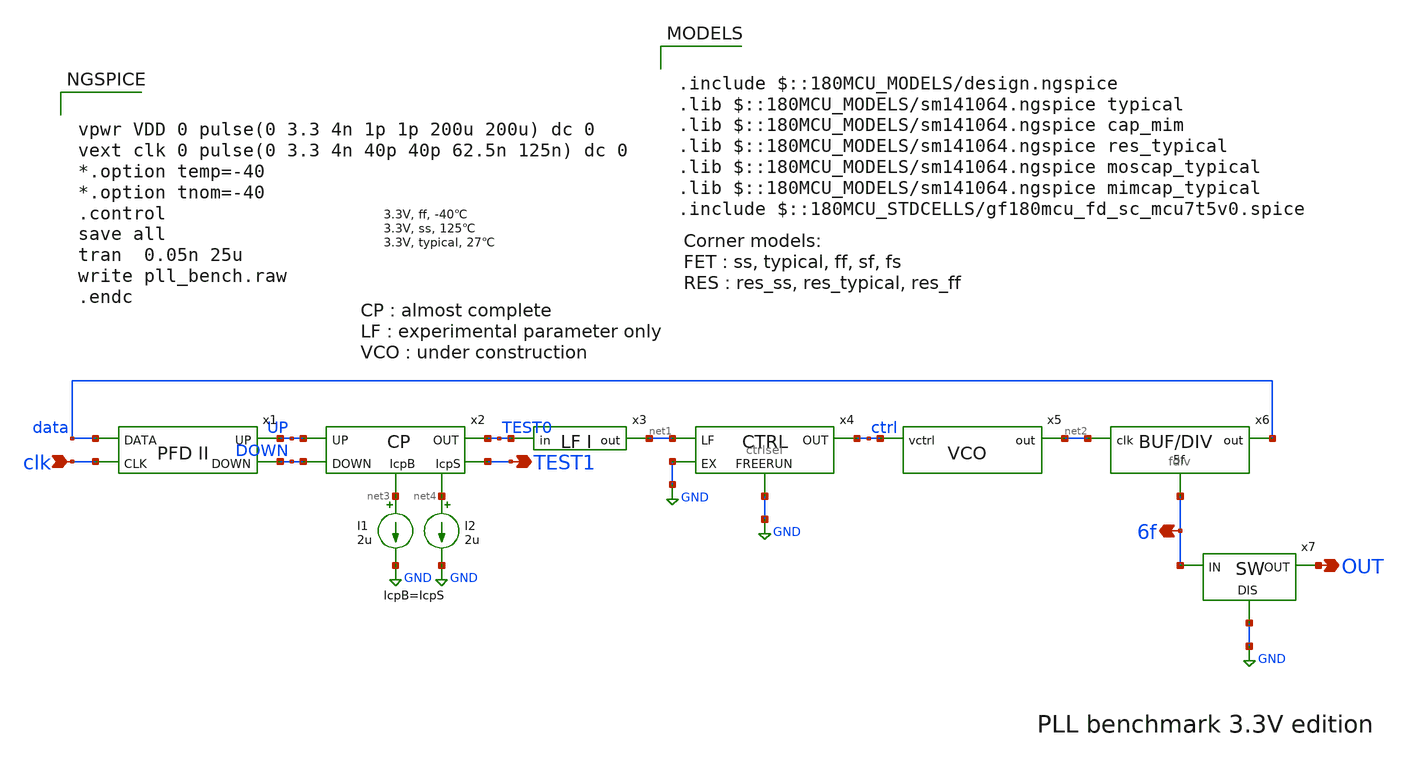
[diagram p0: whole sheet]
** sch_path: PLL/xschem/pll_bench.sch
**.subckt pll_bench clk OUT 6f TEST1
*.ipin clk
*.opin OUT
*.opin 6f
*.opin TEST1
x2 UP DOWN TEST0 net3 net4 TEST1 cp
x5 ctrl net2 vco
x3 net1 TEST0 lf
x4 GND GND ctrl net1 ctrlsel
x7 6f OUT GND sw
x1 data UP DOWN clk pfd2
I2 net4 GND 2u
I1 net3 GND 2u
x6 data net2 6f fdiv
**** begin user architecture code


vpwr VDD 0 pulse(0 3.3 4n 1p 1p 200u 200u) dc 0
vext clk 0 pulse(0 3.3 4n 40p 40p 62.5n 125n) dc 0
*.option temp=-40
*.option tnom=-40
.control
save all
tran  0.05n 25u
write pll_bench.raw
.endc



.include $::180MCU_MODELS/design.ngspice
.lib $::180MCU_MODELS/sm141064.ngspice typical
.lib $::180MCU_MODELS/sm141064.ngspice cap_mim
.lib $::180MCU_MODELS/sm141064.ngspice res_typical
.lib $::180MCU_MODELS/sm141064.ngspice moscap_typical
.lib $::180MCU_MODELS/sm141064.ngspice mimcap_typical
.include $::180MCU_STDCELLS/gf180mcu_fd_sc_mcu7t5v0.spice

**** end user architecture code
**.ends

* expanding   symbol:  cp.sym # of pins=6
** sym_path: PLL/xschem/cp.sym
** sch_path: PLL/xschem/cp.sch
.subckt cp UP DOWN OUT IcpB IcpS VF
*.iopin IcpS
*.iopin IcpB
*.ipin DOWN
*.ipin UP
*.opin OUT
*.opin VF
XM29 net17 OUT net19 VDD pfet_03v3 L=0.33u W=8u nf=1 ad='int((nf+1)/2) * W/nf * 0.18u' as='int((nf+2)/2) * W/nf * 0.18u'
+ pd='2*int((nf+1)/2) * (W/nf + 0.18u)' ps='2*int((nf+2)/2) * (W/nf + 0.18u)' nrd='0.18u / W' nrs='0.18u / W'
+ sa=0 sb=0 sd=0 m=1
XM32 net16 VF net19 VDD pfet_03v3 L=0.33u W=8u nf=1 ad='int((nf+1)/2) * W/nf * 0.18u' as='int((nf+2)/2) * W/nf * 0.18u'
+ pd='2*int((nf+1)/2) * (W/nf + 0.18u)' ps='2*int((nf+2)/2) * (W/nf + 0.18u)' nrd='0.18u / W' nrs='0.18u / W'
+ sa=0 sb=0 sd=0 m=1
XM15 VF UP net3 VDD pfet_03v3 L=0.33u W=8u nf=1 ad='int((nf+1)/2) * W/nf * 0.18u' as='int((nf+2)/2) * W/nf * 0.18u'
+ pd='2*int((nf+1)/2) * (W/nf + 0.18u)' ps='2*int((nf+2)/2) * (W/nf + 0.18u)' nrd='0.18u / W' nrs='0.18u / W'
+ sa=0 sb=0 sd=0 m=1
XM16 VF net2 net4 GND nfet_03v3 L=0.33u W=4u nf=1 ad='int((nf+1)/2) * W/nf * 0.18u' as='int((nf+2)/2) * W/nf * 0.18u'
+ pd='2*int((nf+1)/2) * (W/nf + 0.18u)' ps='2*int((nf+2)/2) * (W/nf + 0.18u)' nrd='0.18u / W' nrs='0.18u / W'
+ sa=0 sb=0 sd=0 m=1
XM11 net2 DOWN VDD VDD pfet_03v3 L=0.33u W=2u nf=1 ad='int((nf+1)/2) * W/nf * 0.18u' as='int((nf+2)/2) * W/nf * 0.18u'
+ pd='2*int((nf+1)/2) * (W/nf + 0.18u)' ps='2*int((nf+2)/2) * (W/nf + 0.18u)' nrd='0.18u / W' nrs='0.18u / W'
+ sa=0 sb=0 sd=0 m=1
XM12 net2 DOWN GND GND nfet_03v3 L=0.33u W=1u nf=1 ad='int((nf+1)/2) * W/nf * 0.18u' as='int((nf+2)/2) * W/nf * 0.18u'
+ pd='2*int((nf+1)/2) * (W/nf + 0.18u)' ps='2*int((nf+2)/2) * (W/nf + 0.18u)' nrd='0.18u / W' nrs='0.18u / W'
+ sa=0 sb=0 sd=0 m=1
XM17 net4 net11 net7 GND nfet_03v3 L=0.33u W=1u nf=1 ad='int((nf+1)/2) * W/nf * 0.18u' as='int((nf+2)/2) * W/nf * 0.18u'
+ pd='2*int((nf+1)/2) * (W/nf + 0.18u)' ps='2*int((nf+2)/2) * (W/nf + 0.18u)' nrd='0.18u / W' nrs='0.18u / W'
+ sa=0 sb=0 sd=0 m=1
XM18 net7 net12 GND GND nfet_03v3 L=0.33u W=1u nf=1 ad='int((nf+1)/2) * W/nf * 0.18u' as='int((nf+2)/2) * W/nf * 0.18u'
+ pd='2*int((nf+1)/2) * (W/nf + 0.18u)' ps='2*int((nf+2)/2) * (W/nf + 0.18u)' nrd='0.18u / W' nrs='0.18u / W'
+ sa=0 sb=0 sd=0 m=1
XM27 net14 IcpS VDD VDD pfet_03v3 L=0.33u W=4u nf=1 ad='int((nf+1)/2) * W/nf * 0.18u' as='int((nf+2)/2) * W/nf * 0.18u'
+ pd='2*int((nf+1)/2) * (W/nf + 0.18u)' ps='2*int((nf+2)/2) * (W/nf + 0.18u)' nrd='0.18u / W' nrs='0.18u / W'
+ sa=0 sb=0 sd=0 m=1
XM28 net19 IcpB net14 VDD pfet_03v3 L=0.33u W=4u nf=1 ad='int((nf+1)/2) * W/nf * 0.18u' as='int((nf+2)/2) * W/nf * 0.18u'
+ pd='2*int((nf+1)/2) * (W/nf + 0.18u)' ps='2*int((nf+2)/2) * (W/nf + 0.18u)' nrd='0.18u / W' nrs='0.18u / W'
+ sa=0 sb=0 sd=0 m=1
XM2 net6 IcpS VDD VDD pfet_03v3 L=0.33u W=4u nf=1 ad='int((nf+1)/2) * W/nf * 0.18u' as='int((nf+2)/2) * W/nf * 0.18u'
+ pd='2*int((nf+1)/2) * (W/nf + 0.18u)' ps='2*int((nf+2)/2) * (W/nf + 0.18u)' nrd='0.18u / W' nrs='0.18u / W'
+ sa=0 sb=0 sd=0 m=1
XM3 IcpS IcpB net6 VDD pfet_03v3 L=0.33u W=4u nf=1 ad='int((nf+1)/2) * W/nf * 0.18u' as='int((nf+2)/2) * W/nf * 0.18u'
+ pd='2*int((nf+1)/2) * (W/nf + 0.18u)' ps='2*int((nf+2)/2) * (W/nf + 0.18u)' nrd='0.18u / W' nrs='0.18u / W'
+ sa=0 sb=0 sd=0 m=1
XM1 IcpB IcpB VDD VDD pfet_03v3 L=0.33u W=0.8u nf=1 ad='int((nf+1)/2) * W/nf * 0.18u' as='int((nf+2)/2) * W/nf * 0.18u'
+ pd='2*int((nf+1)/2) * (W/nf + 0.18u)' ps='2*int((nf+2)/2) * (W/nf + 0.18u)' nrd='0.18u / W' nrs='0.18u / W'
+ sa=0 sb=0 sd=0 m=1
XM9 net12 net11 net8 GND nfet_03v3 L=0.33u W=2u nf=1 ad='int((nf+1)/2) * W/nf * 0.18u' as='int((nf+2)/2) * W/nf * 0.18u'
+ pd='2*int((nf+1)/2) * (W/nf + 0.18u)' ps='2*int((nf+2)/2) * (W/nf + 0.18u)' nrd='0.18u / W' nrs='0.18u / W'
+ sa=0 sb=0 sd=0 m=1
XM10 net8 net12 GND GND nfet_03v3 L=0.33u W=2u nf=1 ad='int((nf+1)/2) * W/nf * 0.18u' as='int((nf+2)/2) * W/nf * 0.18u'
+ pd='2*int((nf+1)/2) * (W/nf + 0.18u)' ps='2*int((nf+2)/2) * (W/nf + 0.18u)' nrd='0.18u / W' nrs='0.18u / W'
+ sa=0 sb=0 sd=0 m=1
XM7 net9 IcpS VDD VDD pfet_03v3 L=0.33u W=4u nf=1 ad='int((nf+1)/2) * W/nf * 0.18u' as='int((nf+2)/2) * W/nf * 0.18u'
+ pd='2*int((nf+1)/2) * (W/nf + 0.18u)' ps='2*int((nf+2)/2) * (W/nf + 0.18u)' nrd='0.18u / W' nrs='0.18u / W'
+ sa=0 sb=0 sd=0 m=1
XM8 net12 IcpB net9 VDD pfet_03v3 L=0.33u W=4u nf=1 ad='int((nf+1)/2) * W/nf * 0.18u' as='int((nf+2)/2) * W/nf * 0.18u'
+ pd='2*int((nf+1)/2) * (W/nf + 0.18u)' ps='2*int((nf+2)/2) * (W/nf + 0.18u)' nrd='0.18u / W' nrs='0.18u / W'
+ sa=0 sb=0 sd=0 m=1
XM4 net10 IcpS VDD VDD pfet_03v3 L=0.33u W=4u nf=1 ad='int((nf+1)/2) * W/nf * 0.18u' as='int((nf+2)/2) * W/nf * 0.18u'
+ pd='2*int((nf+1)/2) * (W/nf + 0.18u)' ps='2*int((nf+2)/2) * (W/nf + 0.18u)' nrd='0.18u / W' nrs='0.18u / W'
+ sa=0 sb=0 sd=0 m=1
XM5 net11 IcpB net10 VDD pfet_03v3 L=0.33u W=4u nf=1 ad='int((nf+1)/2) * W/nf * 0.18u' as='int((nf+2)/2) * W/nf * 0.18u'
+ pd='2*int((nf+1)/2) * (W/nf + 0.18u)' ps='2*int((nf+2)/2) * (W/nf + 0.18u)' nrd='0.18u / W' nrs='0.18u / W'
+ sa=0 sb=0 sd=0 m=1
XM6 net11 net11 GND GND nfet_03v3 L=0.33u W=0.4u nf=1 ad='int((nf+1)/2) * W/nf * 0.18u' as='int((nf+2)/2) * W/nf * 0.18u'
+ pd='2*int((nf+1)/2) * (W/nf + 0.18u)' ps='2*int((nf+2)/2) * (W/nf + 0.18u)' nrd='0.18u / W' nrs='0.18u / W'
+ sa=0 sb=0 sd=0 m=1
XM43 net22 net11 net16 GND nfet_03v3 L=0.33u W=2u nf=1 ad='int((nf+1)/2) * W/nf * 0.18u' as='int((nf+2)/2) * W/nf * 0.18u'
+ pd='2*int((nf+1)/2) * (W/nf + 0.18u)' ps='2*int((nf+2)/2) * (W/nf + 0.18u)' nrd='0.18u / W' nrs='0.18u / W'
+ sa=0 sb=0 sd=0 m=1
XM39 net15 net21 VDD VDD pfet_03v3 L=0.33u W=8u nf=1 ad='int((nf+1)/2) * W/nf * 0.18u' as='int((nf+2)/2) * W/nf * 0.18u'
+ pd='2*int((nf+1)/2) * (W/nf + 0.18u)' ps='2*int((nf+2)/2) * (W/nf + 0.18u)' nrd='0.18u / W' nrs='0.18u / W'
+ sa=0 sb=0 sd=0 m=1
XM44 net16 net22 GND GND nfet_03v3 L=0.33u W=4u nf=1 ad='int((nf+1)/2) * W/nf * 0.18u' as='int((nf+2)/2) * W/nf * 0.18u'
+ pd='2*int((nf+1)/2) * (W/nf + 0.18u)' ps='2*int((nf+2)/2) * (W/nf + 0.18u)' nrd='0.18u / W' nrs='0.18u / W'
+ sa=0 sb=0 sd=0 m=1
XM45 net18 net21 VDD VDD pfet_03v3 L=0.33u W=8u nf=1 ad='int((nf+1)/2) * W/nf * 0.18u' as='int((nf+2)/2) * W/nf * 0.18u'
+ pd='2*int((nf+1)/2) * (W/nf + 0.18u)' ps='2*int((nf+2)/2) * (W/nf + 0.18u)' nrd='0.18u / W' nrs='0.18u / W'
+ sa=0 sb=0 sd=0 m=1
XM46 net24 IcpB net18 VDD pfet_03v3 L=0.33u W=4u nf=1 ad='int((nf+1)/2) * W/nf * 0.18u' as='int((nf+2)/2) * W/nf * 0.18u'
+ pd='2*int((nf+1)/2) * (W/nf + 0.18u)' ps='2*int((nf+2)/2) * (W/nf + 0.18u)' nrd='0.18u / W' nrs='0.18u / W'
+ sa=0 sb=0 sd=0 m=1
XM49 net34 net11 net17 GND nfet_03v3 L=0.33u W=2u nf=1 ad='int((nf+1)/2) * W/nf * 0.18u' as='int((nf+2)/2) * W/nf * 0.18u'
+ pd='2*int((nf+1)/2) * (W/nf + 0.18u)' ps='2*int((nf+2)/2) * (W/nf + 0.18u)' nrd='0.18u / W' nrs='0.18u / W'
+ sa=0 sb=0 sd=0 m=1
XM50 net17 net22 GND GND nfet_03v3 L=0.33u W=4u nf=1 ad='int((nf+1)/2) * W/nf * 0.18u' as='int((nf+2)/2) * W/nf * 0.18u'
+ pd='2*int((nf+1)/2) * (W/nf + 0.18u)' ps='2*int((nf+2)/2) * (W/nf + 0.18u)' nrd='0.18u / W' nrs='0.18u / W'
+ sa=0 sb=0 sd=0 m=1
XM34 net20 net11 net13 GND nfet_03v3 L=0.33u W=2u nf=1 ad='int((nf+1)/2) * W/nf * 0.18u' as='int((nf+2)/2) * W/nf * 0.18u'
+ pd='2*int((nf+1)/2) * (W/nf + 0.18u)' ps='2*int((nf+2)/2) * (W/nf + 0.18u)' nrd='0.18u / W' nrs='0.18u / W'
+ sa=0 sb=0 sd=0 m=1
XM35 net13 net12 GND GND nfet_03v3 L=0.33u W=2u nf=1 ad='int((nf+1)/2) * W/nf * 0.18u' as='int((nf+2)/2) * W/nf * 0.18u'
+ pd='2*int((nf+1)/2) * (W/nf + 0.18u)' ps='2*int((nf+2)/2) * (W/nf + 0.18u)' nrd='0.18u / W' nrs='0.18u / W'
+ sa=0 sb=0 sd=0 m=1
XM33 net18 OUT net20 GND nfet_03v3 L=0.33u W=4u nf=1 ad='int((nf+1)/2) * W/nf * 0.18u' as='int((nf+2)/2) * W/nf * 0.18u'
+ pd='2*int((nf+1)/2) * (W/nf + 0.18u)' ps='2*int((nf+2)/2) * (W/nf + 0.18u)' nrd='0.18u / W' nrs='0.18u / W'
+ sa=0 sb=0 sd=0 m=1
XM36 net15 VF net20 GND nfet_03v3 L=0.33u W=4u nf=1 ad='int((nf+1)/2) * W/nf * 0.18u' as='int((nf+2)/2) * W/nf * 0.18u'
+ pd='2*int((nf+1)/2) * (W/nf + 0.18u)' ps='2*int((nf+2)/2) * (W/nf + 0.18u)' nrd='0.18u / W' nrs='0.18u / W'
+ sa=0 sb=0 sd=0 m=1
XM41 net22 net33 net21 VDD pfet_03v3 L=0.33u W=2u nf=1 ad='int((nf+1)/2) * W/nf * 0.18u' as='int((nf+2)/2) * W/nf * 0.18u'
+ pd='2*int((nf+1)/2) * (W/nf + 0.18u)' ps='2*int((nf+2)/2) * (W/nf + 0.18u)' nrd='0.18u / W' nrs='0.18u / W'
+ sa=0 sb=0 sd=0 m=1
XM42 net21 net23 net22 GND nfet_03v3 L=0.33u W=1u nf=1 ad='int((nf+1)/2) * W/nf * 0.18u' as='int((nf+2)/2) * W/nf * 0.18u'
+ pd='2*int((nf+1)/2) * (W/nf + 0.18u)' ps='2*int((nf+2)/2) * (W/nf + 0.18u)' nrd='0.18u / W' nrs='0.18u / W'
+ sa=0 sb=0 sd=0 m=1
XM47 net34 net33 net24 VDD pfet_03v3 L=0.33u W=2u nf=1 ad='int((nf+1)/2) * W/nf * 0.18u' as='int((nf+2)/2) * W/nf * 0.18u'
+ pd='2*int((nf+1)/2) * (W/nf + 0.18u)' ps='2*int((nf+2)/2) * (W/nf + 0.18u)' nrd='0.18u / W' nrs='0.18u / W'
+ sa=0 sb=0 sd=0 m=1
XM48 net24 net23 net34 GND nfet_03v3 L=0.33u W=1u nf=1 ad='int((nf+1)/2) * W/nf * 0.18u' as='int((nf+2)/2) * W/nf * 0.18u'
+ pd='2*int((nf+1)/2) * (W/nf + 0.18u)' ps='2*int((nf+2)/2) * (W/nf + 0.18u)' nrd='0.18u / W' nrs='0.18u / W'
+ sa=0 sb=0 sd=0 m=1
XM61 VF net24 VDD VDD pfet_03v3 L=0.33u W=8u nf=1 ad='int((nf+1)/2) * W/nf * 0.18u' as='int((nf+2)/2) * W/nf * 0.18u'
+ pd='2*int((nf+1)/2) * (W/nf + 0.18u)' ps='2*int((nf+2)/2) * (W/nf + 0.18u)' nrd='0.18u / W' nrs='0.18u / W'
+ sa=0 sb=0 sd=0 m=1
XM51 net25 net26 VDD VDD pfet_03v3 L=0.33u W=4u nf=1 ad='int((nf+1)/2) * W/nf * 0.18u' as='int((nf+2)/2) * W/nf * 0.18u'
+ pd='2*int((nf+1)/2) * (W/nf + 0.18u)' ps='2*int((nf+2)/2) * (W/nf + 0.18u)' nrd='0.18u / W' nrs='0.18u / W'
+ sa=0 sb=0 sd=0 m=1
XM52 net26 IcpB net25 VDD pfet_03v3 L=0.33u W=4u nf=1 ad='int((nf+1)/2) * W/nf * 0.18u' as='int((nf+2)/2) * W/nf * 0.18u'
+ pd='2*int((nf+1)/2) * (W/nf + 0.18u)' ps='2*int((nf+2)/2) * (W/nf + 0.18u)' nrd='0.18u / W' nrs='0.18u / W'
+ sa=0 sb=0 sd=0 m=1
XM53 net33 net33 net26 VDD pfet_03v3 L=0.33u W=4u nf=1 ad='int((nf+1)/2) * W/nf * 0.18u' as='int((nf+2)/2) * W/nf * 0.18u'
+ pd='2*int((nf+1)/2) * (W/nf + 0.18u)' ps='2*int((nf+2)/2) * (W/nf + 0.18u)' nrd='0.18u / W' nrs='0.18u / W'
+ sa=0 sb=0 sd=0 m=1
XM54 net33 net11 net27 GND nfet_03v3 L=0.33u W=2u nf=1 ad='int((nf+1)/2) * W/nf * 0.18u' as='int((nf+2)/2) * W/nf * 0.18u'
+ pd='2*int((nf+1)/2) * (W/nf + 0.18u)' ps='2*int((nf+2)/2) * (W/nf + 0.18u)' nrd='0.18u / W' nrs='0.18u / W'
+ sa=0 sb=0 sd=0 m=1
XM55 net27 net12 GND GND nfet_03v3 L=0.33u W=2u nf=1 ad='int((nf+1)/2) * W/nf * 0.18u' as='int((nf+2)/2) * W/nf * 0.18u'
+ pd='2*int((nf+1)/2) * (W/nf + 0.18u)' ps='2*int((nf+2)/2) * (W/nf + 0.18u)' nrd='0.18u / W' nrs='0.18u / W'
+ sa=0 sb=0 sd=0 m=1
XM56 net28 IcpS VDD VDD pfet_03v3 L=0.33u W=4u nf=1 ad='int((nf+1)/2) * W/nf * 0.18u' as='int((nf+2)/2) * W/nf * 0.18u'
+ pd='2*int((nf+1)/2) * (W/nf + 0.18u)' ps='2*int((nf+2)/2) * (W/nf + 0.18u)' nrd='0.18u / W' nrs='0.18u / W'
+ sa=0 sb=0 sd=0 m=1
XM57 net23 IcpB net28 VDD pfet_03v3 L=0.33u W=4u nf=1 ad='int((nf+1)/2) * W/nf * 0.18u' as='int((nf+2)/2) * W/nf * 0.18u'
+ pd='2*int((nf+1)/2) * (W/nf + 0.18u)' ps='2*int((nf+2)/2) * (W/nf + 0.18u)' nrd='0.18u / W' nrs='0.18u / W'
+ sa=0 sb=0 sd=0 m=1
XM59 net30 net11 net29 GND nfet_03v3 L=0.33u W=2u nf=1 ad='int((nf+1)/2) * W/nf * 0.18u' as='int((nf+2)/2) * W/nf * 0.18u'
+ pd='2*int((nf+1)/2) * (W/nf + 0.18u)' ps='2*int((nf+2)/2) * (W/nf + 0.18u)' nrd='0.18u / W' nrs='0.18u / W'
+ sa=0 sb=0 sd=0 m=1
XM60 net29 net30 GND GND nfet_03v3 L=0.33u W=2u nf=1 ad='int((nf+1)/2) * W/nf * 0.18u' as='int((nf+2)/2) * W/nf * 0.18u'
+ pd='2*int((nf+1)/2) * (W/nf + 0.18u)' ps='2*int((nf+2)/2) * (W/nf + 0.18u)' nrd='0.18u / W' nrs='0.18u / W'
+ sa=0 sb=0 sd=0 m=1
XM58 net23 net23 net30 GND nfet_03v3 L=0.33u W=2u nf=1 ad='int((nf+1)/2) * W/nf * 0.18u' as='int((nf+2)/2) * W/nf * 0.18u'
+ pd='2*int((nf+1)/2) * (W/nf + 0.18u)' ps='2*int((nf+2)/2) * (W/nf + 0.18u)' nrd='0.18u / W' nrs='0.18u / W'
+ sa=0 sb=0 sd=0 m=1
XM62 VF net34 GND GND nfet_03v3 L=0.33u W=4u nf=1 ad='int((nf+1)/2) * W/nf * 0.18u' as='int((nf+2)/2) * W/nf * 0.18u'
+ pd='2*int((nf+1)/2) * (W/nf + 0.18u)' ps='2*int((nf+2)/2) * (W/nf + 0.18u)' nrd='0.18u / W' nrs='0.18u / W'
+ sa=0 sb=0 sd=0 m=1
XM30 net31 IcpS VDD VDD pfet_03v3 L=0.33u W=4u nf=1 ad='int((nf+1)/2) * W/nf * 0.18u' as='int((nf+2)/2) * W/nf * 0.18u'
+ pd='2*int((nf+1)/2) * (W/nf + 0.18u)' ps='2*int((nf+2)/2) * (W/nf + 0.18u)' nrd='0.18u / W' nrs='0.18u / W'
+ sa=0 sb=0 sd=0 m=1
XM31 net19 IcpB net31 VDD pfet_03v3 L=0.33u W=4u nf=1 ad='int((nf+1)/2) * W/nf * 0.18u' as='int((nf+2)/2) * W/nf * 0.18u'
+ pd='2*int((nf+1)/2) * (W/nf + 0.18u)' ps='2*int((nf+2)/2) * (W/nf + 0.18u)' nrd='0.18u / W' nrs='0.18u / W'
+ sa=0 sb=0 sd=0 m=1
XM37 net20 net11 net32 GND nfet_03v3 L=0.33u W=2u nf=1 ad='int((nf+1)/2) * W/nf * 0.18u' as='int((nf+2)/2) * W/nf * 0.18u'
+ pd='2*int((nf+1)/2) * (W/nf + 0.18u)' ps='2*int((nf+2)/2) * (W/nf + 0.18u)' nrd='0.18u / W' nrs='0.18u / W'
+ sa=0 sb=0 sd=0 m=1
XM38 net32 net12 GND GND nfet_03v3 L=0.33u W=2u nf=1 ad='int((nf+1)/2) * W/nf * 0.18u' as='int((nf+2)/2) * W/nf * 0.18u'
+ pd='2*int((nf+1)/2) * (W/nf + 0.18u)' ps='2*int((nf+2)/2) * (W/nf + 0.18u)' nrd='0.18u / W' nrs='0.18u / W'
+ sa=0 sb=0 sd=0 m=1
C1 net18 VF 280f m=1
C2 VF net17 280f m=1
XM13 net35 IcpS VDD VDD pfet_03v3 L=0.33u W=2u nf=1 ad='int((nf+1)/2) * W/nf * 0.18u' as='int((nf+2)/2) * W/nf * 0.18u'
+ pd='2*int((nf+1)/2) * (W/nf + 0.18u)' ps='2*int((nf+2)/2) * (W/nf + 0.18u)' nrd='0.18u / W' nrs='0.18u / W'
+ sa=0 sb=0 sd=0 m=1
XM14 net3 IcpB net35 VDD pfet_03v3 L=0.33u W=2u nf=1 ad='int((nf+1)/2) * W/nf * 0.18u' as='int((nf+2)/2) * W/nf * 0.18u'
+ pd='2*int((nf+1)/2) * (W/nf + 0.18u)' ps='2*int((nf+2)/2) * (W/nf + 0.18u)' nrd='0.18u / W' nrs='0.18u / W'
+ sa=0 sb=0 sd=0 m=1
XM19 net5 IcpS VDD VDD pfet_03v3 L=0.33u W=2u nf=1 ad='int((nf+1)/2) * W/nf * 0.18u' as='int((nf+2)/2) * W/nf * 0.18u'
+ pd='2*int((nf+1)/2) * (W/nf + 0.18u)' ps='2*int((nf+2)/2) * (W/nf + 0.18u)' nrd='0.18u / W' nrs='0.18u / W'
+ sa=0 sb=0 sd=0 m=1
XM20 net3 IcpB net5 VDD pfet_03v3 L=0.33u W=2u nf=1 ad='int((nf+1)/2) * W/nf * 0.18u' as='int((nf+2)/2) * W/nf * 0.18u'
+ pd='2*int((nf+1)/2) * (W/nf + 0.18u)' ps='2*int((nf+2)/2) * (W/nf + 0.18u)' nrd='0.18u / W' nrs='0.18u / W'
+ sa=0 sb=0 sd=0 m=1
XM21 OUT net1 net3 VDD pfet_03v3 L=0.33u W=8u nf=1 ad='int((nf+1)/2) * W/nf * 0.18u' as='int((nf+2)/2) * W/nf * 0.18u'
+ pd='2*int((nf+1)/2) * (W/nf + 0.18u)' ps='2*int((nf+2)/2) * (W/nf + 0.18u)' nrd='0.18u / W' nrs='0.18u / W'
+ sa=0 sb=0 sd=0 m=1
XM22 OUT DOWN net4 GND nfet_03v3 L=0.33u W=4u nf=1 ad='int((nf+1)/2) * W/nf * 0.18u' as='int((nf+2)/2) * W/nf * 0.18u'
+ pd='2*int((nf+1)/2) * (W/nf + 0.18u)' ps='2*int((nf+2)/2) * (W/nf + 0.18u)' nrd='0.18u / W' nrs='0.18u / W'
+ sa=0 sb=0 sd=0 m=1
XM23 net4 net11 net36 GND nfet_03v3 L=0.33u W=1u nf=1 ad='int((nf+1)/2) * W/nf * 0.18u' as='int((nf+2)/2) * W/nf * 0.18u'
+ pd='2*int((nf+1)/2) * (W/nf + 0.18u)' ps='2*int((nf+2)/2) * (W/nf + 0.18u)' nrd='0.18u / W' nrs='0.18u / W'
+ sa=0 sb=0 sd=0 m=1
XM24 net36 net12 GND GND nfet_03v3 L=0.33u W=1u nf=1 ad='int((nf+1)/2) * W/nf * 0.18u' as='int((nf+2)/2) * W/nf * 0.18u'
+ pd='2*int((nf+1)/2) * (W/nf + 0.18u)' ps='2*int((nf+2)/2) * (W/nf + 0.18u)' nrd='0.18u / W' nrs='0.18u / W'
+ sa=0 sb=0 sd=0 m=1
XM25 net1 UP VDD VDD pfet_03v3 L=0.33u W=2u nf=1 ad='int((nf+1)/2) * W/nf * 0.18u' as='int((nf+2)/2) * W/nf * 0.18u'
+ pd='2*int((nf+1)/2) * (W/nf + 0.18u)' ps='2*int((nf+2)/2) * (W/nf + 0.18u)' nrd='0.18u / W' nrs='0.18u / W'
+ sa=0 sb=0 sd=0 m=1
XM26 net1 UP GND GND nfet_03v3 L=0.33u W=1u nf=1 ad='int((nf+1)/2) * W/nf * 0.18u' as='int((nf+2)/2) * W/nf * 0.18u'
+ pd='2*int((nf+1)/2) * (W/nf + 0.18u)' ps='2*int((nf+2)/2) * (W/nf + 0.18u)' nrd='0.18u / W' nrs='0.18u / W'
+ sa=0 sb=0 sd=0 m=1
XM40 net21 IcpB net15 VDD pfet_03v3 L=0.33u W=4u nf=1 ad='int((nf+1)/2) * W/nf * 0.18u' as='int((nf+2)/2) * W/nf * 0.18u'
+ pd='2*int((nf+1)/2) * (W/nf + 0.18u)' ps='2*int((nf+2)/2) * (W/nf + 0.18u)' nrd='0.18u / W' nrs='0.18u / W'
+ sa=0 sb=0 sd=0 m=1
.ends


* expanding   symbol:  vco.sym # of pins=2
** sym_path: PLL/xschem/vco.sym
** sch_path: PLL/xschem/vco.sch
.subckt vco vctrl out
*.ipin vctrl
*.opin out
XM2 net1 net1 VDD VDD pfet_03v3 L=0.33u W=2u nf=1 ad='int((nf+1)/2) * W/nf * 0.18u' as='int((nf+2)/2) * W/nf * 0.18u'
+ pd='2*int((nf+1)/2) * (W/nf + 0.18u)' ps='2*int((nf+2)/2) * (W/nf + 0.18u)' nrd='0.18u / W' nrs='0.18u / W'
+ sa=0 sb=0 sd=0 m=1
XM4 net2 net1 VDD VDD pfet_03v3 L=0.33u W=2u nf=1 ad='int((nf+1)/2) * W/nf * 0.18u' as='int((nf+2)/2) * W/nf * 0.18u'
+ pd='2*int((nf+1)/2) * (W/nf + 0.18u)' ps='2*int((nf+2)/2) * (W/nf + 0.18u)' nrd='0.18u / W' nrs='0.18u / W'
+ sa=0 sb=0 sd=0 m=1
XM1 net2 net2 GND GND nfet_03v3 L=0.33u W=0.8u nf=1 ad='int((nf+1)/2) * W/nf * 0.18u' as='int((nf+2)/2) * W/nf * 0.18u'
+ pd='2*int((nf+1)/2) * (W/nf + 0.18u)' ps='2*int((nf+2)/2) * (W/nf + 0.18u)' nrd='0.18u / W' nrs='0.18u / W'
+ sa=0 sb=0 sd=0 m=1
XM5 net6 net1 VDD VDD pfet_03v3 L=0.33u W=2u nf=1 ad='int((nf+1)/2) * W/nf * 0.18u' as='int((nf+2)/2) * W/nf * 0.18u'
+ pd='2*int((nf+1)/2) * (W/nf + 0.18u)' ps='2*int((nf+2)/2) * (W/nf + 0.18u)' nrd='0.18u / W' nrs='0.18u / W'
+ sa=0 sb=0 sd=0 m=1
XM6 net5 net2 GND GND nfet_03v3 L=0.33u W=0.8u nf=1 ad='int((nf+1)/2) * W/nf * 0.18u' as='int((nf+2)/2) * W/nf * 0.18u'
+ pd='2*int((nf+1)/2) * (W/nf + 0.18u)' ps='2*int((nf+2)/2) * (W/nf + 0.18u)' nrd='0.18u / W' nrs='0.18u / W'
+ sa=0 sb=0 sd=0 m=1
I1 VDD net3 2u
XM8 net3 net3 GND GND nfet_03v3 L=0.33u W=0.8u nf=1 ad='int((nf+1)/2) * W/nf * 0.18u' as='int((nf+2)/2) * W/nf * 0.18u'
+ pd='2*int((nf+1)/2) * (W/nf + 0.18u)' ps='2*int((nf+2)/2) * (W/nf + 0.18u)' nrd='0.18u / W' nrs='0.18u / W'
+ sa=0 sb=0 sd=0 m=1
R1 net21 GND 240k m=1
XM3 net1 vctrl net21 GND nfet_03v3 L=0.28u W=0.8u nf=1 ad='int((nf+1)/2) * W/nf * 0.18u' as='int((nf+2)/2) * W/nf * 0.18u'
+ pd='2*int((nf+1)/2) * (W/nf + 0.18u)' ps='2*int((nf+2)/2) * (W/nf + 0.18u)' nrd='0.18u / W' nrs='0.18u / W'
+ sa=0 sb=0 sd=0 m=1
XM7 net1 net3 GND GND nfet_03v3 L=0.33u W=2.4u nf=1 ad='int((nf+1)/2) * W/nf * 0.18u' as='int((nf+2)/2) * W/nf * 0.18u'
+ pd='2*int((nf+1)/2) * (W/nf + 0.18u)' ps='2*int((nf+2)/2) * (W/nf + 0.18u)' nrd='0.18u / W' nrs='0.18u / W'
+ sa=0 sb=0 sd=0 m=1
XM9 net4 out net6 VDD pfet_03v3 L=0.33u W=4u nf=1 ad='int((nf+1)/2) * W/nf * 0.18u' as='int((nf+2)/2) * W/nf * 0.18u'
+ pd='2*int((nf+1)/2) * (W/nf + 0.18u)' ps='2*int((nf+2)/2) * (W/nf + 0.18u)' nrd='0.18u / W' nrs='0.18u / W'
+ sa=0 sb=0 sd=0 m=1
XM10 net4 out net5 GND nfet_03v3 L=0.33u W=1.6u nf=1 ad='int((nf+1)/2) * W/nf * 0.18u' as='int((nf+2)/2) * W/nf * 0.18u'
+ pd='2*int((nf+1)/2) * (W/nf + 0.18u)' ps='2*int((nf+2)/2) * (W/nf + 0.18u)' nrd='0.18u / W' nrs='0.18u / W'
+ sa=0 sb=0 sd=0 m=1
XM11 net9 net1 VDD VDD pfet_03v3 L=0.33u W=2u nf=1 ad='int((nf+1)/2) * W/nf * 0.18u' as='int((nf+2)/2) * W/nf * 0.18u'
+ pd='2*int((nf+1)/2) * (W/nf + 0.18u)' ps='2*int((nf+2)/2) * (W/nf + 0.18u)' nrd='0.18u / W' nrs='0.18u / W'
+ sa=0 sb=0 sd=0 m=1
XM12 net8 net2 GND GND nfet_03v3 L=0.33u W=0.8u nf=1 ad='int((nf+1)/2) * W/nf * 0.18u' as='int((nf+2)/2) * W/nf * 0.18u'
+ pd='2*int((nf+1)/2) * (W/nf + 0.18u)' ps='2*int((nf+2)/2) * (W/nf + 0.18u)' nrd='0.18u / W' nrs='0.18u / W'
+ sa=0 sb=0 sd=0 m=1
XM13 net7 net4 net9 VDD pfet_03v3 L=0.33u W=4u nf=1 ad='int((nf+1)/2) * W/nf * 0.18u' as='int((nf+2)/2) * W/nf * 0.18u'
+ pd='2*int((nf+1)/2) * (W/nf + 0.18u)' ps='2*int((nf+2)/2) * (W/nf + 0.18u)' nrd='0.18u / W' nrs='0.18u / W'
+ sa=0 sb=0 sd=0 m=1
XM14 net7 net4 net8 GND nfet_03v3 L=0.33u W=1.6u nf=1 ad='int((nf+1)/2) * W/nf * 0.18u' as='int((nf+2)/2) * W/nf * 0.18u'
+ pd='2*int((nf+1)/2) * (W/nf + 0.18u)' ps='2*int((nf+2)/2) * (W/nf + 0.18u)' nrd='0.18u / W' nrs='0.18u / W'
+ sa=0 sb=0 sd=0 m=1
XM15 net12 net1 VDD VDD pfet_03v3 L=0.33u W=2u nf=1 ad='int((nf+1)/2) * W/nf * 0.18u' as='int((nf+2)/2) * W/nf * 0.18u'
+ pd='2*int((nf+1)/2) * (W/nf + 0.18u)' ps='2*int((nf+2)/2) * (W/nf + 0.18u)' nrd='0.18u / W' nrs='0.18u / W'
+ sa=0 sb=0 sd=0 m=1
XM16 net11 net2 GND GND nfet_03v3 L=0.33u W=0.8u nf=1 ad='int((nf+1)/2) * W/nf * 0.18u' as='int((nf+2)/2) * W/nf * 0.18u'
+ pd='2*int((nf+1)/2) * (W/nf + 0.18u)' ps='2*int((nf+2)/2) * (W/nf + 0.18u)' nrd='0.18u / W' nrs='0.18u / W'
+ sa=0 sb=0 sd=0 m=1
XM17 net10 net7 net12 VDD pfet_03v3 L=0.33u W=4u nf=1 ad='int((nf+1)/2) * W/nf * 0.18u' as='int((nf+2)/2) * W/nf * 0.18u'
+ pd='2*int((nf+1)/2) * (W/nf + 0.18u)' ps='2*int((nf+2)/2) * (W/nf + 0.18u)' nrd='0.18u / W' nrs='0.18u / W'
+ sa=0 sb=0 sd=0 m=1
XM18 net10 net7 net11 GND nfet_03v3 L=0.33u W=1.6u nf=1 ad='int((nf+1)/2) * W/nf * 0.18u' as='int((nf+2)/2) * W/nf * 0.18u'
+ pd='2*int((nf+1)/2) * (W/nf + 0.18u)' ps='2*int((nf+2)/2) * (W/nf + 0.18u)' nrd='0.18u / W' nrs='0.18u / W'
+ sa=0 sb=0 sd=0 m=1
XM19 net15 net1 VDD VDD pfet_03v3 L=0.33u W=2u nf=1 ad='int((nf+1)/2) * W/nf * 0.18u' as='int((nf+2)/2) * W/nf * 0.18u'
+ pd='2*int((nf+1)/2) * (W/nf + 0.18u)' ps='2*int((nf+2)/2) * (W/nf + 0.18u)' nrd='0.18u / W' nrs='0.18u / W'
+ sa=0 sb=0 sd=0 m=1
XM20 net14 net2 GND GND nfet_03v3 L=0.33u W=0.8u nf=1 ad='int((nf+1)/2) * W/nf * 0.18u' as='int((nf+2)/2) * W/nf * 0.18u'
+ pd='2*int((nf+1)/2) * (W/nf + 0.18u)' ps='2*int((nf+2)/2) * (W/nf + 0.18u)' nrd='0.18u / W' nrs='0.18u / W'
+ sa=0 sb=0 sd=0 m=1
XM21 net13 net10 net15 VDD pfet_03v3 L=0.33u W=4u nf=1 ad='int((nf+1)/2) * W/nf * 0.18u' as='int((nf+2)/2) * W/nf * 0.18u'
+ pd='2*int((nf+1)/2) * (W/nf + 0.18u)' ps='2*int((nf+2)/2) * (W/nf + 0.18u)' nrd='0.18u / W' nrs='0.18u / W'
+ sa=0 sb=0 sd=0 m=1
XM22 net13 net10 net14 GND nfet_03v3 L=0.33u W=1.6u nf=1 ad='int((nf+1)/2) * W/nf * 0.18u' as='int((nf+2)/2) * W/nf * 0.18u'
+ pd='2*int((nf+1)/2) * (W/nf + 0.18u)' ps='2*int((nf+2)/2) * (W/nf + 0.18u)' nrd='0.18u / W' nrs='0.18u / W'
+ sa=0 sb=0 sd=0 m=1
XM23 net17 net1 VDD VDD pfet_03v3 L=0.33u W=2u nf=1 ad='int((nf+1)/2) * W/nf * 0.18u' as='int((nf+2)/2) * W/nf * 0.18u'
+ pd='2*int((nf+1)/2) * (W/nf + 0.18u)' ps='2*int((nf+2)/2) * (W/nf + 0.18u)' nrd='0.18u / W' nrs='0.18u / W'
+ sa=0 sb=0 sd=0 m=1
XM24 net16 net2 GND GND nfet_03v3 L=0.33u W=0.8u nf=1 ad='int((nf+1)/2) * W/nf * 0.18u' as='int((nf+2)/2) * W/nf * 0.18u'
+ pd='2*int((nf+1)/2) * (W/nf + 0.18u)' ps='2*int((nf+2)/2) * (W/nf + 0.18u)' nrd='0.18u / W' nrs='0.18u / W'
+ sa=0 sb=0 sd=0 m=1
XM25 out net13 net17 VDD pfet_03v3 L=0.33u W=4u nf=1 ad='int((nf+1)/2) * W/nf * 0.18u' as='int((nf+2)/2) * W/nf * 0.18u'
+ pd='2*int((nf+1)/2) * (W/nf + 0.18u)' ps='2*int((nf+2)/2) * (W/nf + 0.18u)' nrd='0.18u / W' nrs='0.18u / W'
+ sa=0 sb=0 sd=0 m=1
XM26 out net13 net16 GND nfet_03v3 L=0.33u W=1.6u nf=1 ad='int((nf+1)/2) * W/nf * 0.18u' as='int((nf+2)/2) * W/nf * 0.18u'
+ pd='2*int((nf+1)/2) * (W/nf + 0.18u)' ps='2*int((nf+2)/2) * (W/nf + 0.18u)' nrd='0.18u / W' nrs='0.18u / W'
+ sa=0 sb=0 sd=0 m=1
XM27 net20 net1 VDD VDD pfet_03v3 L=0.33u W=2u nf=1 ad='int((nf+1)/2) * W/nf * 0.18u' as='int((nf+2)/2) * W/nf * 0.18u'
+ pd='2*int((nf+1)/2) * (W/nf + 0.18u)' ps='2*int((nf+2)/2) * (W/nf + 0.18u)' nrd='0.18u / W' nrs='0.18u / W'
+ sa=0 sb=0 sd=0 m=1
XM28 net19 net2 GND GND nfet_03v3 L=0.33u W=0.8u nf=1 ad='int((nf+1)/2) * W/nf * 0.18u' as='int((nf+2)/2) * W/nf * 0.18u'
+ pd='2*int((nf+1)/2) * (W/nf + 0.18u)' ps='2*int((nf+2)/2) * (W/nf + 0.18u)' nrd='0.18u / W' nrs='0.18u / W'
+ sa=0 sb=0 sd=0 m=1
XM29 net18 out net20 VDD pfet_03v3 L=0.33u W=4u nf=1 ad='int((nf+1)/2) * W/nf * 0.18u' as='int((nf+2)/2) * W/nf * 0.18u'
+ pd='2*int((nf+1)/2) * (W/nf + 0.18u)' ps='2*int((nf+2)/2) * (W/nf + 0.18u)' nrd='0.18u / W' nrs='0.18u / W'
+ sa=0 sb=0 sd=0 m=1
XM30 net18 out net19 GND nfet_03v3 L=0.33u W=1.6u nf=1 ad='int((nf+1)/2) * W/nf * 0.18u' as='int((nf+2)/2) * W/nf * 0.18u'
+ pd='2*int((nf+1)/2) * (W/nf + 0.18u)' ps='2*int((nf+2)/2) * (W/nf + 0.18u)' nrd='0.18u / W' nrs='0.18u / W'
+ sa=0 sb=0 sd=0 m=1
.ends


* expanding   symbol:  lf.sym # of pins=2
** sym_path: PLL/xschem/lf.sym
** sch_path: PLL/xschem/lf.sch
.subckt lf out in
*.ipin in
*.opin out
R2 net1 GND 451k m=1
C1 in GND 242f m=1
C2 in net1 2660f m=1
R3 out in 577k m=1
C3 out GND 173f m=1
.ends


* expanding   symbol:  ctrlsel.sym # of pins=4
** sym_path: PLL/xschem/ctrlsel.sym
** sch_path: PLL/xschem/ctrlsel.sch
.subckt ctrlsel EX FREERUN OUT LF
*.opin OUT
*.ipin EX
*.ipin LF
*.ipin FREERUN
x1 FREERUN net1 VDD VDD 0 0 gf180mcu_fd_sc_mcu7t5v0__inv_1
x2 net1 OUT EX FREERUN tmg
x3 FREERUN OUT LF net1 tmg
.ends


* expanding   symbol:  sw.sym # of pins=3
** sym_path: PLL/xschem/sw.sym
** sch_path: PLL/xschem/sw.sch
.subckt sw IN OUT DIS
*.opin OUT
*.ipin IN
*.ipin DIS
x1 DIS net1 VDD VDD GND GND gf180mcu_fd_sc_mcu7t5v0__inv_1
x2 DIS OUT IN net1 tmg
.ends


* expanding   symbol:  pfd2.sym # of pins=4
** sym_path: PLL/xschem/pfd2.sym
** sch_path: PLL/xschem/pfd2.sch
.subckt pfd2 DATA UP DOWN CLK
*.ipin DATA
*.ipin CLK
*.opin UP
*.opin DOWN
x1 net9 net8 net1 VDD VDD 0 0 gf180mcu_fd_sc_mcu7t5v0__nand2_1
x7 CLK net8 VDD VDD 0 0 gf180mcu_fd_sc_mcu7t5v0__clkinv_1
x2 net1 net7 net6 VDD VDD 0 0 gf180mcu_fd_sc_mcu7t5v0__nand2_1
x3 net6 net5 net7 VDD VDD 0 0 gf180mcu_fd_sc_mcu7t5v0__nand2_1
x4 net5 net4 net3 VDD VDD 0 0 gf180mcu_fd_sc_mcu7t5v0__nand2_1
x5 net3 net2 net4 VDD VDD 0 0 gf180mcu_fd_sc_mcu7t5v0__nand2_1
x6 net10 net15 net2 VDD VDD 0 0 gf180mcu_fd_sc_mcu7t5v0__nand2_1
x8 DATA net10 VDD VDD 0 0 gf180mcu_fd_sc_mcu7t5v0__clkinv_1
x13 net14 net6 net5 net9 VDD VDD 0 0 gf180mcu_fd_sc_mcu7t5v0__nand3_1
x14 net5 net4 net13 net15 VDD VDD 0 0 gf180mcu_fd_sc_mcu7t5v0__nand3_1
x15 net1 net6 net4 net2 net5 VDD VDD 0 0 gf180mcu_fd_sc_mcu7t5v0__nand4_1
x9 net1 net11 VDD VDD 0 0 gf180mcu_fd_sc_mcu7t5v0__clkinv_1
x10 net11 net14 VDD VDD 0 0 gf180mcu_fd_sc_mcu7t5v0__clkinv_1
x11 net2 net12 VDD VDD 0 0 gf180mcu_fd_sc_mcu7t5v0__clkinv_1
x12 net12 net13 VDD VDD 0 0 gf180mcu_fd_sc_mcu7t5v0__clkinv_1
x16 net9 UP VDD VDD 0 0 gf180mcu_fd_sc_mcu7t5v0__clkinv_1
x17 net15 DOWN VDD VDD 0 0 gf180mcu_fd_sc_mcu7t5v0__clkinv_1
.ends


* expanding   symbol:  gf180_pll_3v3/fdiv.sym # of pins=3
** sym_path: PLL/xschem/fdiv.sym
** sch_path: PLL/xschem/fdiv.sch
.subckt fdiv out clk 5f
*.ipin clk
*.opin out
*.opin 5f
x10 clk net7 VDD VDD 0 0 gf180mcu_fd_sc_mcu7t5v0__clkbuf_3
x11 net7 5f VDD VDD 0 0 gf180mcu_fd_sc_mcu7t5v0__clkbuf_8
x1 net1 5f net2 VDD VDD 0 0 gf180mcu_fd_sc_mcu7t5v0__dffq_1
x7 net3 net4 net1 VDD VDD 0 0 gf180mcu_fd_sc_mcu7t5v0__nand2_1
x2 net2 5f net3 VDD VDD 0 0 gf180mcu_fd_sc_mcu7t5v0__dffq_1
x3 net3 5f net4 VDD VDD 0 0 gf180mcu_fd_sc_mcu7t5v0__dffq_1
x4 net8 net5 net6 VDD VDD 0 0 gf180mcu_fd_sc_mcu7t5v0__dffq_1
x5 net3 net2 net8 VDD VDD 0 0 gf180mcu_fd_sc_mcu7t5v0__or2_1
x6 5f net5 VDD VDD 0 0 gf180mcu_fd_sc_mcu7t5v0__clkinv_1
x8 net4 net6 out VDD VDD 0 0 gf180mcu_fd_sc_mcu7t5v0__nand2_1
.ends


* expanding   symbol:  tmg.sym # of pins=4
** sym_path: PLL/xschem/tmg.sym
** sch_path: PLL/xschem/tmg.sch
.subckt tmg PG B A NG
*.opin B
*.ipin A
*.ipin PG
*.ipin NG
XM3 B PG A VDD pfet_06v0 L=0.50u W=2u nf=1 ad='int((nf+1)/2) * W/nf * 0.18u' as='int((nf+2)/2) * W/nf * 0.18u'
+ pd='2*int((nf+1)/2) * (W/nf + 0.18u)' ps='2*int((nf+2)/2) * (W/nf + 0.18u)' nrd='0.18u / W' nrs='0.18u / W'
+ sa=0 sb=0 sd=0 m=1
XM4 A NG B GND nfet_06v0 L=0.60u W=0.9u nf=1 ad='int((nf+1)/2) * W/nf * 0.18u' as='int((nf+2)/2) * W/nf * 0.18u'
+ pd='2*int((nf+1)/2) * (W/nf + 0.18u)' ps='2*int((nf+2)/2) * (W/nf + 0.18u)' nrd='0.18u / W' nrs='0.18u / W'
+ sa=0 sb=0 sd=0 m=1
.ends

.GLOBAL GND
.GLOBAL VDD
.end
